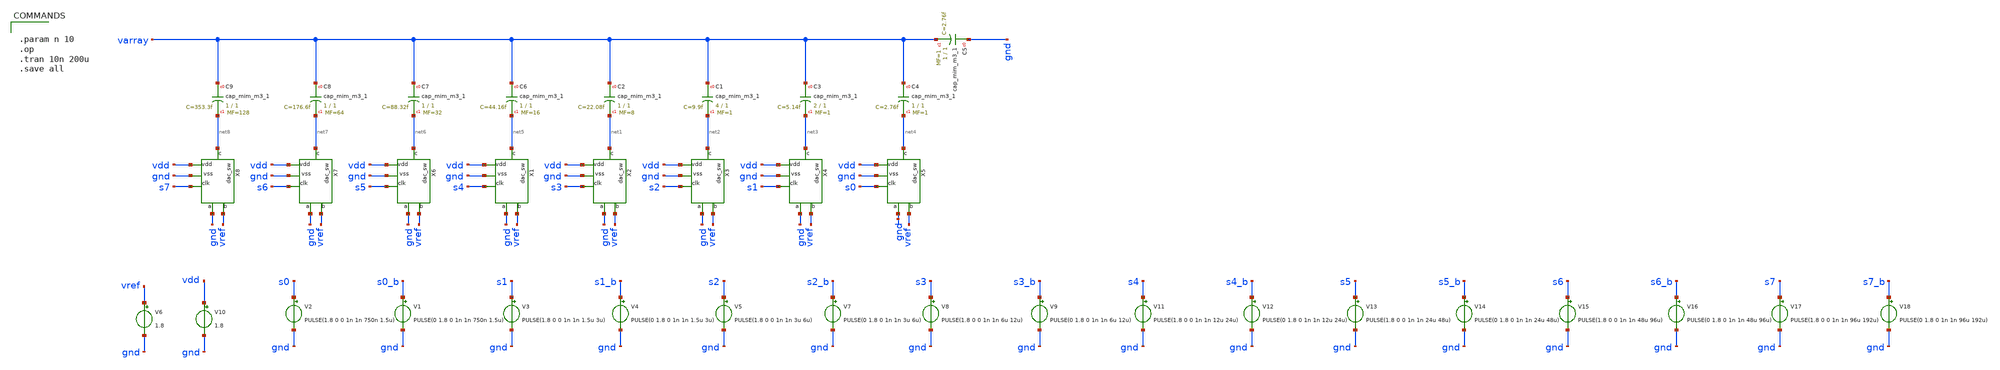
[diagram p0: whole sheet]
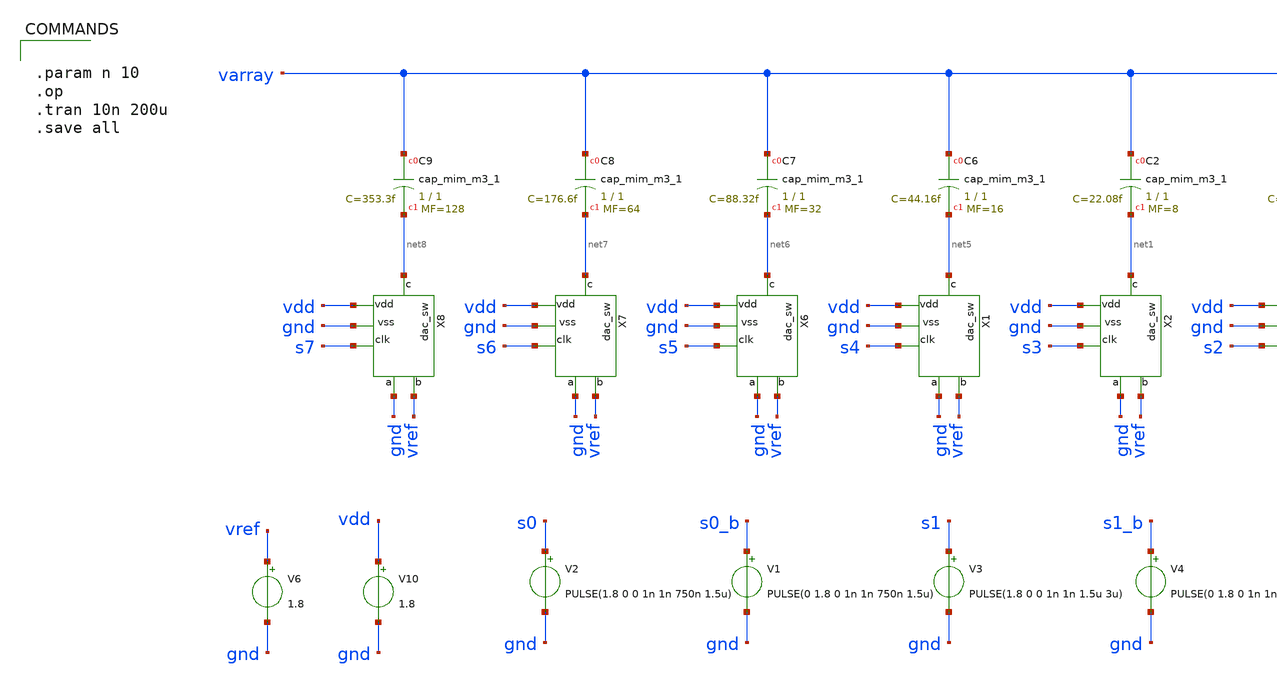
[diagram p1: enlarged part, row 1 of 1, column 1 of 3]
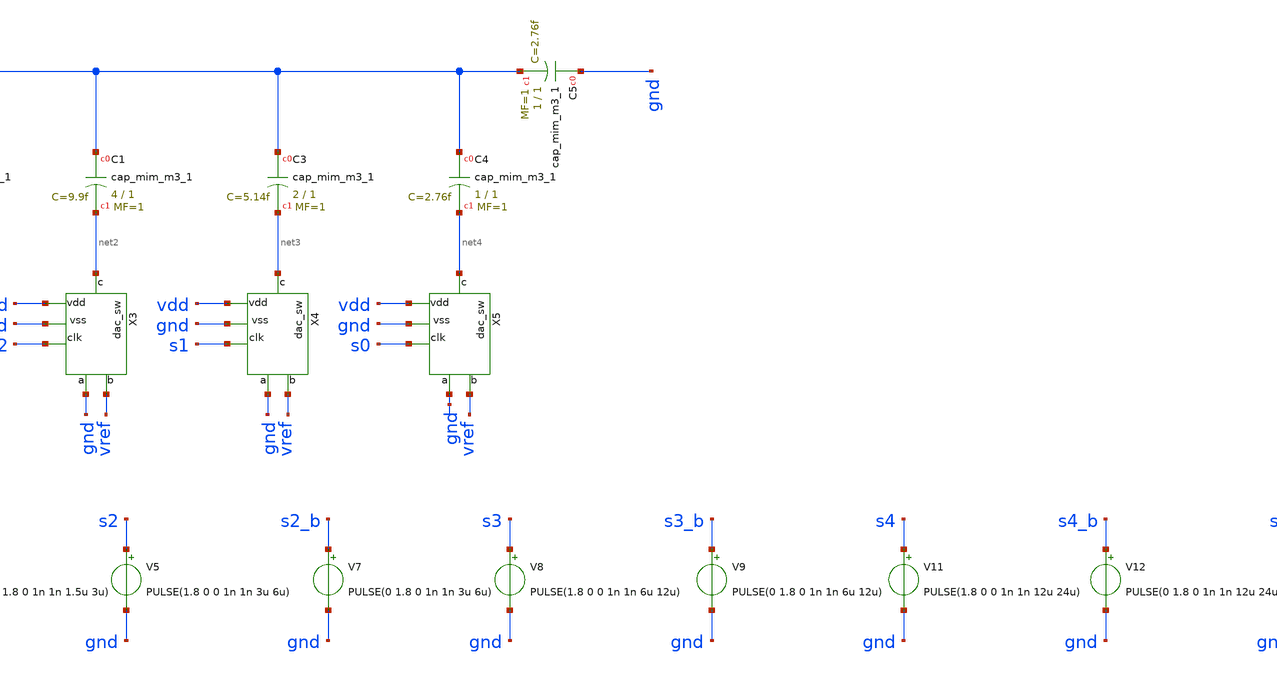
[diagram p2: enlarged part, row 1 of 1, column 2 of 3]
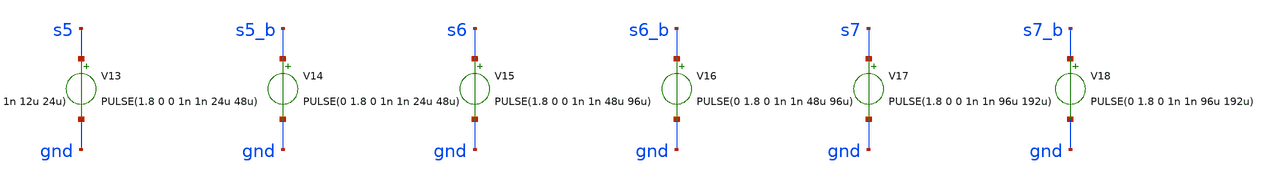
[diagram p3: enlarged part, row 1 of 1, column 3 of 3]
** sch_path: xschem/dac/dac_tb.sch
.lib $::SKYWATER_MODELS/sky130.lib.spice tt
.include $::SKYWATER_STDCELLS/sky130_fd_sc_hd.spice

**.subckt dac_tb
XC2 varray net1 sky130_fd_pr__cap_mim_m3_1 W=1 L=1 MF=8 m=8
V2 s0 gnd PULSE(1.8 0 0 1n 1n 750n 1.5u)
V6 vref gnd 1.8
V1 s0_b gnd PULSE(0 1.8 0 1n 1n 750n 1.5u)
V3 s1 gnd PULSE(1.8 0 0 1n 1n 1.5u 3u)
V4 s1_b gnd PULSE(0 1.8 0 1n 1n 1.5u 3u)
V5 s2 gnd PULSE(1.8 0 0 1n 1n 3u 6u)
V7 s2_b gnd PULSE(0 1.8 0 1n 1n 3u 6u)
V8 s3 gnd PULSE(1.8 0 0 1n 1n 6u 12u)
V9 s3_b gnd PULSE(0 1.8 0 1n 1n 6u 12u)
V10 vdd gnd 1.8
X2 net1 vref gnd vdd s3 gnd dac_sw
XC1 varray net2 sky130_fd_pr__cap_mim_m3_1 W=4 L=1 MF=1 m=1
X3 net2 vref gnd vdd s2 gnd dac_sw
X4 net3 vref gnd vdd s1 gnd dac_sw
X5 net4 vref gnd vdd s0 gnd dac_sw
XC3 varray net3 sky130_fd_pr__cap_mim_m3_1 W=2 L=1 MF=1 m=1
XC4 varray net4 sky130_fd_pr__cap_mim_m3_1 W=1 L=1 MF=1 m=1
XC5 gnd varray sky130_fd_pr__cap_mim_m3_1 W=1 L=1 MF=1 m=1
XC6 varray net5 sky130_fd_pr__cap_mim_m3_1 W=1 L=1 MF=16 m=16
X1 net5 vref gnd vdd s4 gnd dac_sw
XC7 varray net6 sky130_fd_pr__cap_mim_m3_1 W=1 L=1 MF=32 m=32
X6 net6 vref gnd vdd s5 gnd dac_sw
XC8 varray net7 sky130_fd_pr__cap_mim_m3_1 W=1 L=1 MF=64 m=64
X7 net7 vref gnd vdd s6 gnd dac_sw
XC9 varray net8 sky130_fd_pr__cap_mim_m3_1 W=1 L=1 MF=128 m=128
X8 net8 vref gnd vdd s7 gnd dac_sw
V11 s4 gnd PULSE(1.8 0 0 1n 1n 12u 24u)
V12 s4_b gnd PULSE(0 1.8 0 1n 1n 12u 24u)
V13 s5 gnd PULSE(1.8 0 0 1n 1n 24u 48u)
V14 s5_b gnd PULSE(0 1.8 0 1n 1n 24u 48u)
V15 s6 gnd PULSE(1.8 0 0 1n 1n 48u 96u)
V16 s6_b gnd PULSE(0 1.8 0 1n 1n 48u 96u)
V17 s7 gnd PULSE(1.8 0 0 1n 1n 96u 192u)
V18 s7_b gnd PULSE(0 1.8 0 1n 1n 96u 192u)
**** begin user architecture code


.param n 10
.op
.tran 10n 200u
.save all


**** end user architecture code
**.ends

* expanding   symbol:  xschem/dac/dac_sw.sym # of pins=6
** sym_path: xschem/dac/dac_sw.sym
** sch_path: xschem/dac/dac_sw.sch
.subckt dac_sw c b vss vdd clk a
*.iopin vdd
*.iopin vss
*.ipin clk
*.iopin c
*.iopin a
*.iopin b
XM2 c clk b vss sky130_fd_pr__nfet_01v8 L=0.15 W=10 nf=1 ad='int((nf+1)/2) * W/nf * 0.29' as='int((nf+2)/2) * W/nf * 0.29'
+ pd='2*int((nf+1)/2) * (W/nf + 0.29)' ps='2*int((nf+2)/2) * (W/nf + 0.29)' nrd='0.29 / W' nrs='0.29 / W'
+ sa=0 sb=0 sd=0 mult=1 m=1
XM5 b net1 c vdd sky130_fd_pr__pfet_01v8 L=0.15 W=20 nf=1 ad='int((nf+1)/2) * W/nf * 0.29' as='int((nf+2)/2) * W/nf * 0.29'
+ pd='2*int((nf+1)/2) * (W/nf + 0.29)' ps='2*int((nf+2)/2) * (W/nf + 0.29)' nrd='0.29 / W' nrs='0.29 / W'
+ sa=0 sb=0 sd=0 mult=1 m=1
XM6 c net1 a vss sky130_fd_pr__nfet_01v8 L=0.15 W=10 nf=1 ad='int((nf+1)/2) * W/nf * 0.29' as='int((nf+2)/2) * W/nf * 0.29'
+ pd='2*int((nf+1)/2) * (W/nf + 0.29)' ps='2*int((nf+2)/2) * (W/nf + 0.29)' nrd='0.29 / W' nrs='0.29 / W'
+ sa=0 sb=0 sd=0 mult=1 m=1
XM7 a clk c vdd sky130_fd_pr__pfet_01v8 L=0.15 W=20 nf=1 ad='int((nf+1)/2) * W/nf * 0.29' as='int((nf+2)/2) * W/nf * 0.29'
+ pd='2*int((nf+1)/2) * (W/nf + 0.29)' ps='2*int((nf+2)/2) * (W/nf + 0.29)' nrd='0.29 / W' nrs='0.29 / W'
+ sa=0 sb=0 sd=0 mult=1 m=1
x1 clk vss vss vdd vdd net1 sky130_fd_sc_hd__inv_1
.ends

.end
